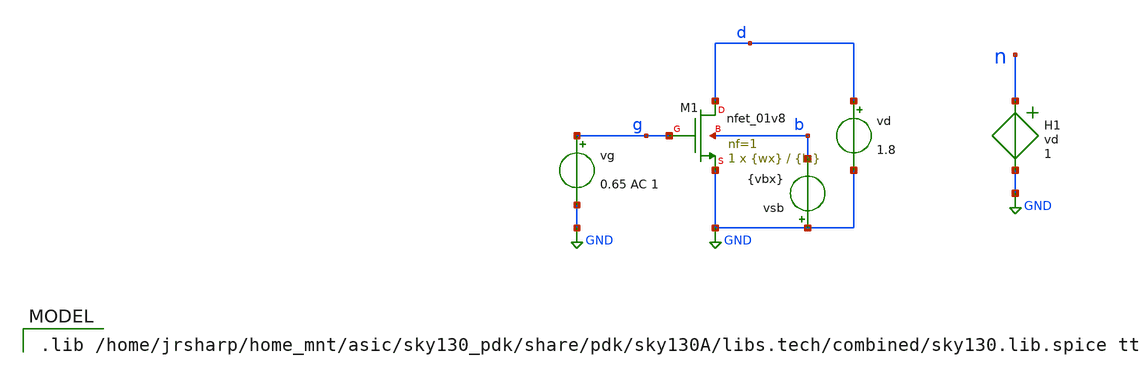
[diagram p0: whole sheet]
** sch_path: 3_1-MOSFET-Characterization/nmos-sweep.sch
**.subckt nmos-sweep
XM1 d g GND b sky130_fd_pr__nfet_01v8 L={lx} W={wx} nf=1 ad='int((nf+1)/2) * W/nf * 0.29' as='int((nf+2)/2) * W/nf * 0.29'
+ pd='2*int((nf+1)/2) * (W/nf + 0.29)' ps='2*int((nf+2)/2) * (W/nf + 0.29)' nrd='0.29 / W' nrs='0.29 / W'
+ sa=0 sb=0 sd=0 mult=1 m=1
vd d GND 1.8
vg g GND 0.65 AC 1
vsb GND b {vbx}
H1 n GND vd 1
**** begin user architecture code

.lib /home/jrsharp/home_mnt/asic/sky130_pdk/share/pdk/sky130A/libs.tech/combined/sky130.lib.spice tt




.temp 27
.option sparse
.param wx=5 lx=0.15 vbx=0
.noise v(n) vg lin 1 1 1 1
.control

option numdgt=3
set wr_singlescale
set wr_vecnames

compose l_vec  values 0.13 0.2 0.3 0.4 0.5 1 5 10
compose vg_vec start= 0 stop=1.5  step=25m
compose vd_vec start= 0 stop=1.5  step=25m
compose vb_vec values 0 0.4 0.8 1.2

foreach var1 $&l_vec
  alterparam lx=$var1
  reset
  foreach var2 $&vg_vec
    alter vg $var2
    foreach var3 $&vd_vec
      alter vd $var3
      foreach var4 $&vb_vec
        alter vsb $var4
	run
	wrdata techsweep_sky13_lv_nmos.txt noise1.all
	destroy all
	set appendwrite
	unset set wr_vecnames
      end
    end
  end
end

set appendwrite=0

alterparam lx=0.15
alterparam vbx=0
reset
op
*showmod
show
write techsweep_sky130_lv_nmos.raw

*quit
.endc

.save b d g n
.save @m.XM1.msky130_fd_pr__nfet_01v8[id]
.save @m.XM1.msky130_fd_pr__nfet_01v8[gm]
.save @m.XM1.msky130_fd_pr__nfet_01v8[gds]
.save @m.XM1.msky130_fd_pr__nfet_01v8[vth]
.save @m.XM1.msky130_fd_pr__nfet_01v8[cgg]
.save @m.XM1.msky130_fd_pr__nfet_01v8[cgd]
*.save @m.XM1.msky130_fd_pr__nfet_01v8[vdss]
*.save @m.XM1.msky130_fd_pr__nfet_01v8[fug]
*.save @m.XM1.msky130_fd_pr__nfet_01v8[rg]
*.save @m.XM1.msky130_fd_pr__nfet_01v8[sid]
*.save @m.XM1.msky130_fd_pr__nfet_01v8[cgsol]
*.save @m.XM1.msky130_fd_pr__nfet_01v8[cgdol]
.save @m.XM1.msky130_fd_pr__nfet_01v8[cdd]
.save @m.XM1.msky130_fd_pr__nfet_01v8[cgb]
.save @m.XM1.msky130_fd_pr__nfet_01v8[cgd]
.save @m.XM1.msky130_fd_pr__nfet_01v8[cgg]
.save @m.XM1.msky130_fd_pr__nfet_01v8[cgs]
.save @m.XM1.msky130_fd_pr__nfet_01v8[css]
.save @m.XM1.msky130_fd_pr__nfet_01v8[gds]
.save @m.XM1.msky130_fd_pr__nfet_01v8[gm]
*.save @m.XM1.msky130_fd_pr__nfet_01v8[gmb]
*.save @m.XM1.msky130_fd_pr__nfet_01v8[ids]
.save @m.XM1.msky130_fd_pr__nfet_01v8[l]
.save @m.XM1.msky130_fd_pr__nfet_01v8[w]
.save @m.XM1.msky130_fd_pr__nfet_01v8[vgs]
.save @m.XM1.msky130_fd_pr__nfet_01v8[vds]
*.save @m.XM1.msky130_fd_pr__nfet_01v8[vsb]
.save @m.XM1.msky130_fd_pr__nfet_01v8[vth]
*.save @m.XM1.msky130_fd_pr__nfet_01v8[vdss]
*.save @m.XM1.msky130_fd_pr__nfet_01v8[fug]
*.save @m.XM1.msky130_fd_pr__nfet_01v8[sid]
*.save @m.XM1.msky130_fd_pr__nfet_01v8[sfl]
*.save @m.XM1.msky130_fd_pr__nfet_01v8[cjd]
*.save @m.XM1.msky130_fd_pr__nfet_01v8[cjs]
*.save @m.XM1.msky130_fd_pr__nfet_01v8[rg]



**** end user architecture code
**.ends
.GLOBAL GND
.end
